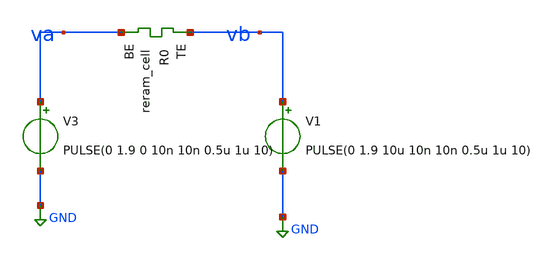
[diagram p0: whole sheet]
** sch_path: Synapse/synapsis.sch
**.subckt synapsis
V1 vb GND PULSE(0 1.9 10u 10n 10n 0.5u 1u 10)
V3 va GND PULSE(0 1.9 0 10n 10n 0.5u 1u 10)
XR0 vb va sky130_fd_pr_reram__reram_cell Tfilament_0=3.8e-9
**** begin user architecture code

** opencircuitdesign pdks install
.inc $::SKYWATER_MODELS/sky130_fd_pr_reram__reram_cell.spice



.options savecurrents
.control
save all
tran 10n 20u
write synapsis.raw
.endc



**** end user architecture code
**.ends
.GLOBAL GND
.end
